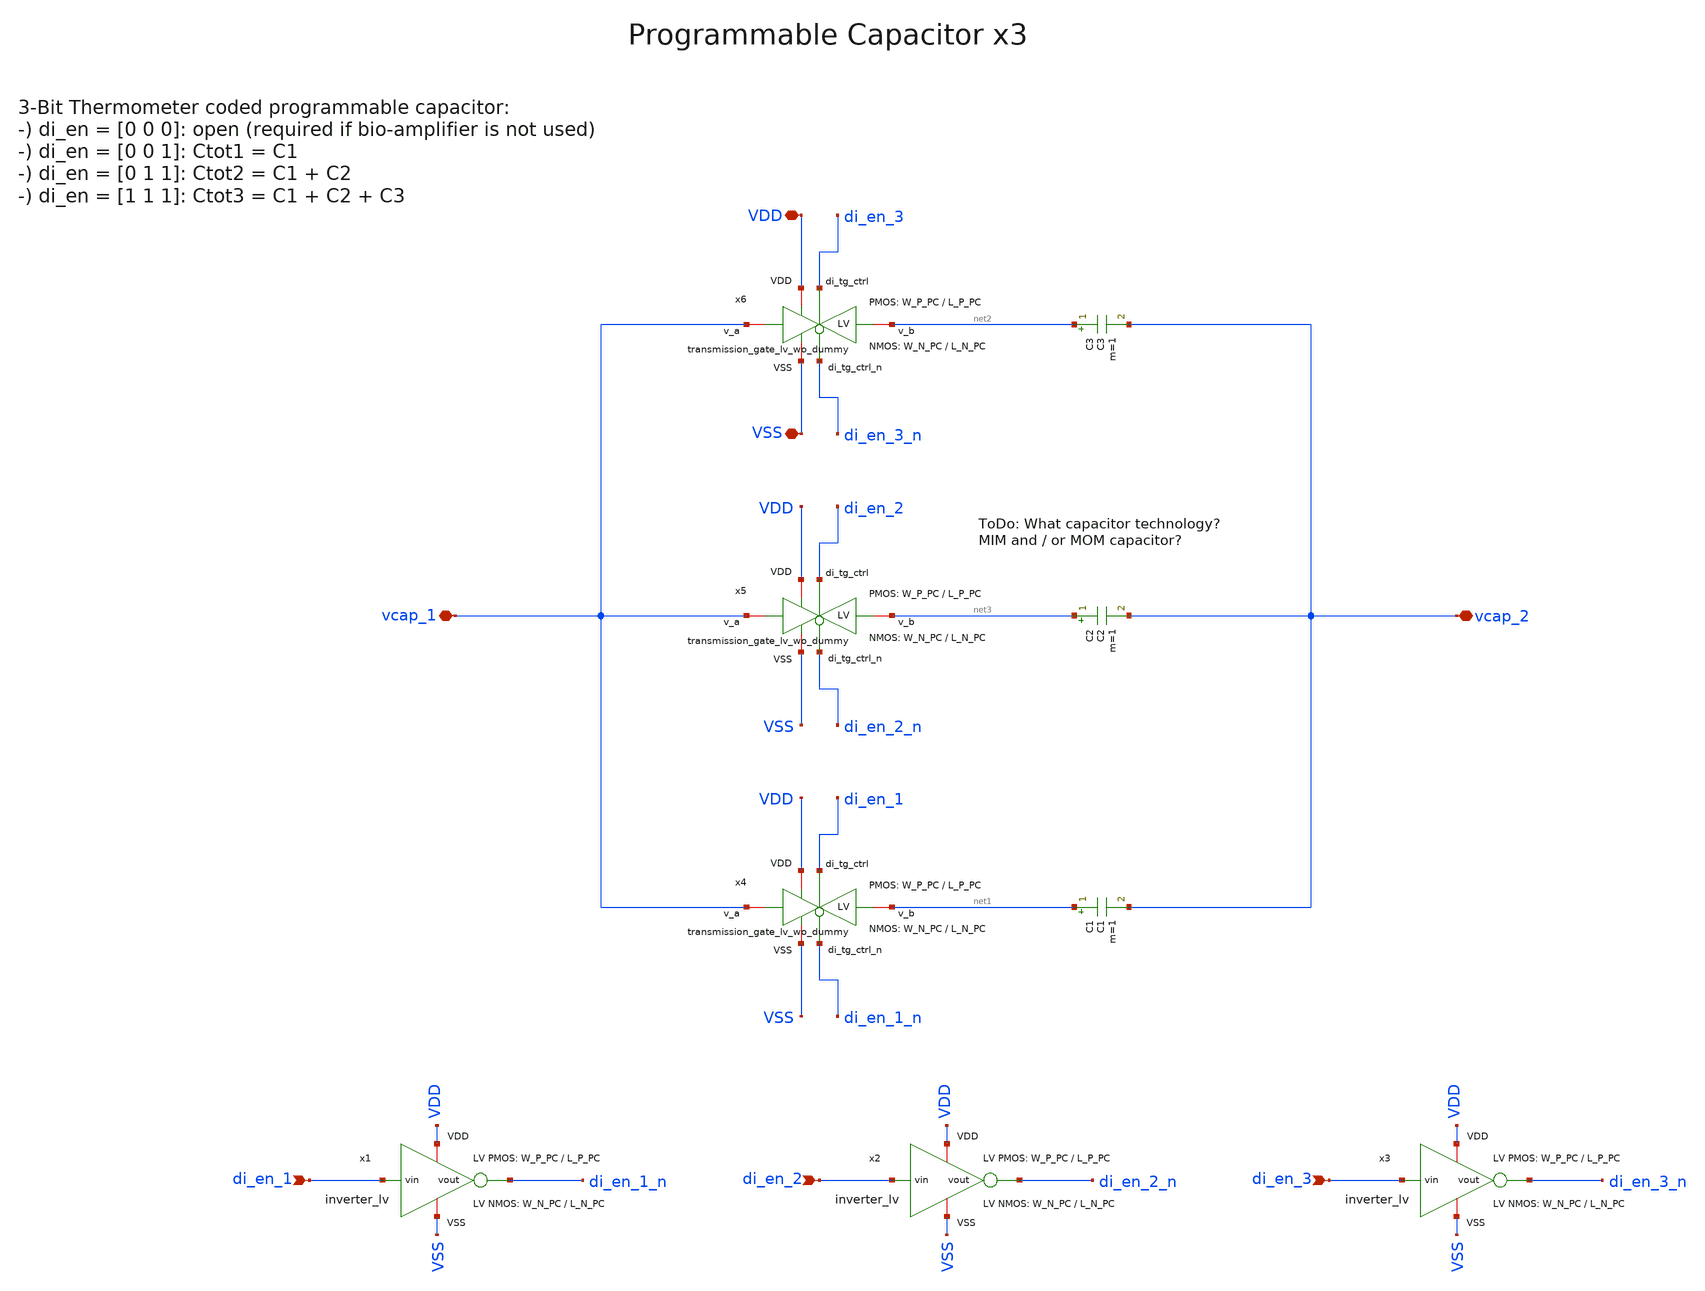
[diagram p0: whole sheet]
** sch_path: SG13G2_ATBS-ADC-main/xschem/programmable_cap/programmable_cap_x3.sch
**.subckt programmable_cap_x3 vcap_1 vcap_2 di_en_1 di_en_2 di_en_3 VDD VSS
*.iopin vcap_1
*.iopin vcap_2
*.ipin di_en_1
*.ipin di_en_2
*.ipin di_en_3
*.iopin VDD
*.iopin VSS
x6 VDD di_en_3 VSS net2 vcap_1 di_en_3_n transmission_gate_lv_wo_dummy W_P=W_P_PC L_P=L_P_PC
+ W_N=W_N_PC L_N=L_N_PC
x5 VDD di_en_2 VSS net3 vcap_1 di_en_2_n transmission_gate_lv_wo_dummy W_P=W_P_PC L_P=L_P_PC
+ W_N=W_N_PC L_N=L_N_PC
x4 VDD di_en_1 VSS net1 vcap_1 di_en_1_n transmission_gate_lv_wo_dummy W_P=W_P_PC L_P=L_P_PC
+ W_N=W_N_PC L_N=L_N_PC
C3 net2 vcap_2 C3 m=1
C2 net3 vcap_2 C2 m=1
C1 net1 vcap_2 C1 m=1
x1 VDD di_en_1 di_en_1_n VSS inverter_lv W_P=W_P_PC L_P=L_P_PC W_N=W_N_PC L_N=L_N_PC
x2 VDD di_en_2 di_en_2_n VSS inverter_lv W_P=W_P_PC L_P=L_P_PC W_N=W_N_PC L_N=L_N_PC
x3 VDD di_en_3 di_en_3_n VSS inverter_lv W_P=W_P_PC L_P=L_P_PC W_N=W_N_PC L_N=L_N_PC
**.ends

* expanding   symbol:  transmission_gate/transmission_gate_lv_wo_dummy.sym # of pins=6
** sym_path: SG13G2_ATBS-ADC-main/xschem/transmission_gate/transmission_gate_lv_wo_dummy.sym
** sch_path: SG13G2_ATBS-ADC-main/xschem/transmission_gate/transmission_gate_lv_wo_dummy.sch
.subckt transmission_gate_lv_wo_dummy VDD di_tg_ctrl VSS v_b v_a di_tg_ctrl_n  W_P=1.0u L_P=0.13u
+ W_N=1.0u L_N=0.13u
*.iopin v_a
*.iopin v_b
*.iopin VDD
*.iopin VSS
*.ipin di_tg_ctrl
*.ipin di_tg_ctrl_n
XM1 v_a di_tg_ctrl v_b VSS sg13_lv_nmos w=W_N l=L_N ng=1 m=1 mm_ok=1
XM2 v_a di_tg_ctrl_n v_b VDD sg13_lv_pmos w=W_P l=L_P ng=1 m=1 mm_ok=1
.ends


* expanding   symbol:  inverter/inverter_lv.sym # of pins=4
** sym_path: SG13G2_ATBS-ADC-main/xschem/inverter/inverter_lv.sym
** sch_path: SG13G2_ATBS-ADC-main/xschem/inverter/inverter_lv.sch
.subckt inverter_lv VDD vin vout VSS  W_P=3.0u L_P=0.13u W_N=1.0u L_N=0.13u
*.ipin vin
*.iopin VDD
*.iopin VSS
*.opin vout
XM1 vout vin VDD VDD sg13_lv_pmos w=W_P l=L_P ng=1 m=1 mm_ok=1
XM2 vout vin VSS VSS sg13_lv_nmos w=W_N l=L_N ng=1 m=1 mm_ok=1
.ends

.end
